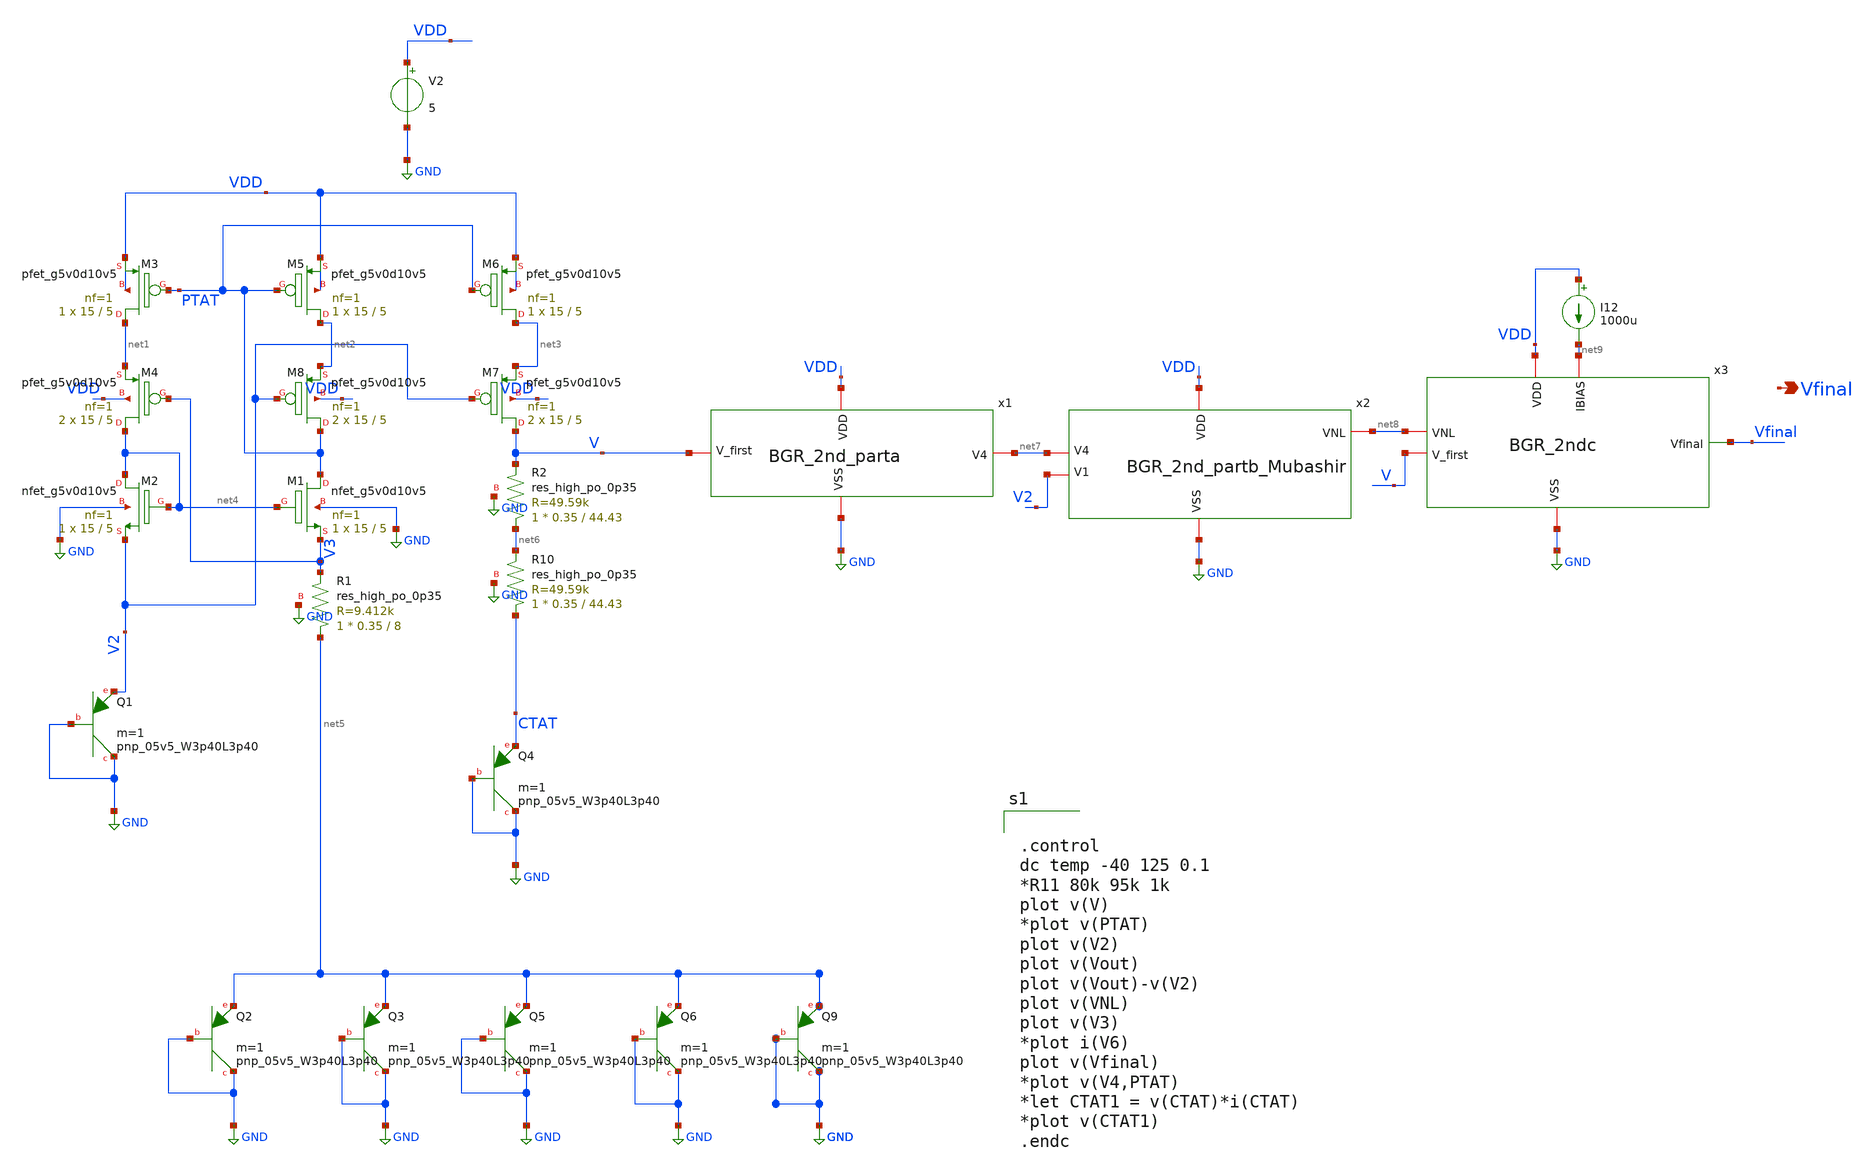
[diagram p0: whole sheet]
** sch_path: xschem/xschem_BGR_Top/BGR_Toplevel_2nd_order.sch
**.subckt BGR_Toplevel_2nd_order Vfinal
*.opin Vfinal
XQ1 GND GND V2 sky130_fd_pr__pnp_05v5_W3p40L3p40 m=1
XQ2 GND GND net5 sky130_fd_pr__pnp_05v5_W3p40L3p40 m=1
XQ3 GND GND net5 sky130_fd_pr__pnp_05v5_W3p40L3p40 m=1
XQ4 GND GND CTAT sky130_fd_pr__pnp_05v5_W3p40L3p40 m=1
V2 VDD GND 5
XM1 PTAT net4 V3 GND sky130_fd_pr__nfet_g5v0d10v5 L=5 W=15 nf=1 ad='int((nf+1)/2) * W/nf * 0.29' as='int((nf+2)/2) * W/nf * 0.29'
+ pd='2*int((nf+1)/2) * (W/nf + 0.29)' ps='2*int((nf+2)/2) * (W/nf + 0.29)' nrd='0.29 / W' nrs='0.29 / W'
+ sa=0 sb=0 sd=0 mult=1 m=1
XM2 net4 net4 V2 GND sky130_fd_pr__nfet_g5v0d10v5 L=5 W=15 nf=1 ad='int((nf+1)/2) * W/nf * 0.29' as='int((nf+2)/2) * W/nf * 0.29'
+ pd='2*int((nf+1)/2) * (W/nf + 0.29)' ps='2*int((nf+2)/2) * (W/nf + 0.29)' nrd='0.29 / W' nrs='0.29 / W'
+ sa=0 sb=0 sd=0 mult=1 m=1
XM3 net1 PTAT VDD VDD sky130_fd_pr__pfet_g5v0d10v5 L=5 W=15 nf=1 ad='int((nf+1)/2) * W/nf * 0.29' as='int((nf+2)/2) * W/nf * 0.29'
+ pd='2*int((nf+1)/2) * (W/nf + 0.29)' ps='2*int((nf+2)/2) * (W/nf + 0.29)' nrd='0.29 / W' nrs='0.29 / W'
+ sa=0 sb=0 sd=0 mult=1 m=1
XM4 net4 V3 net1 VDD sky130_fd_pr__pfet_g5v0d10v5 L=5 W=15 nf=1 ad='int((nf+1)/2) * W/nf * 0.29' as='int((nf+2)/2) * W/nf * 0.29'
+ pd='2*int((nf+1)/2) * (W/nf + 0.29)' ps='2*int((nf+2)/2) * (W/nf + 0.29)' nrd='0.29 / W' nrs='0.29 / W'
+ sa=0 sb=0 sd=0 mult=2 m=2
XM5 net2 PTAT VDD VDD sky130_fd_pr__pfet_g5v0d10v5 L=5 W=15 nf=1 ad='int((nf+1)/2) * W/nf * 0.29' as='int((nf+2)/2) * W/nf * 0.29'
+ pd='2*int((nf+1)/2) * (W/nf + 0.29)' ps='2*int((nf+2)/2) * (W/nf + 0.29)' nrd='0.29 / W' nrs='0.29 / W'
+ sa=0 sb=0 sd=0 mult=1 m=1
XM6 net3 PTAT VDD VDD sky130_fd_pr__pfet_g5v0d10v5 L=5 W=15 nf=1 ad='int((nf+1)/2) * W/nf * 0.29' as='int((nf+2)/2) * W/nf * 0.29'
+ pd='2*int((nf+1)/2) * (W/nf + 0.29)' ps='2*int((nf+2)/2) * (W/nf + 0.29)' nrd='0.29 / W' nrs='0.29 / W'
+ sa=0 sb=0 sd=0 mult=1 m=1
XM7 V V2 net3 VDD sky130_fd_pr__pfet_g5v0d10v5 L=5 W=15 nf=1 ad='int((nf+1)/2) * W/nf * 0.29' as='int((nf+2)/2) * W/nf * 0.29'
+ pd='2*int((nf+1)/2) * (W/nf + 0.29)' ps='2*int((nf+2)/2) * (W/nf + 0.29)' nrd='0.29 / W' nrs='0.29 / W'
+ sa=0 sb=0 sd=0 mult=2 m=2
XM8 PTAT V2 net2 VDD sky130_fd_pr__pfet_g5v0d10v5 L=5 W=15 nf=1 ad='int((nf+1)/2) * W/nf * 0.29' as='int((nf+2)/2) * W/nf * 0.29'
+ pd='2*int((nf+1)/2) * (W/nf + 0.29)' ps='2*int((nf+2)/2) * (W/nf + 0.29)' nrd='0.29 / W' nrs='0.29 / W'
+ sa=0 sb=0 sd=0 mult=2 m=2
XQ5 GND GND net5 sky130_fd_pr__pnp_05v5_W3p40L3p40 m=1
XQ6 GND GND net5 sky130_fd_pr__pnp_05v5_W3p40L3p40 m=1
XR1 net5 V3 GND sky130_fd_pr__res_high_po_0p35 L=8 mult=1 m=1
XR2 net6 V GND sky130_fd_pr__res_high_po_0p35 L=44.43 mult=1 m=1
XQ9 GND GND net5 sky130_fd_pr__pnp_05v5_W3p40L3p40 m=1
XR10 CTAT net6 GND sky130_fd_pr__res_high_po_0p35 L=44.43 mult=1 m=1
x1 VDD GND V net7 BGR_2nd_parta
x3 VDD GND net8 V net9 Vfinal BGR_2ndc
I12 VDD net9 1000u
x2 VDD GND V2 net7 net8 BGR_2nd_partb_Mubashir
**** begin user architecture code

** opencircuitdesign pdks install
.lib $::SKYWATER_MODELS/sky130.lib.spice tt




.control
dc temp -40 125 0.1
*R11 80k 95k 1k
plot v(V)
*plot v(PTAT)
plot v(V2)
plot v(Vout)
plot v(Vout)-v(V2)
plot v(VNL)
plot v(V3)
*plot i(V6)
plot v(Vfinal)
*plot v(V4,PTAT)
*let CTAT1 = v(CTAT)*i(CTAT)
*plot v(CTAT1)
.endc


**** end user architecture code
**.ends
.GLOBAL GND
.end
